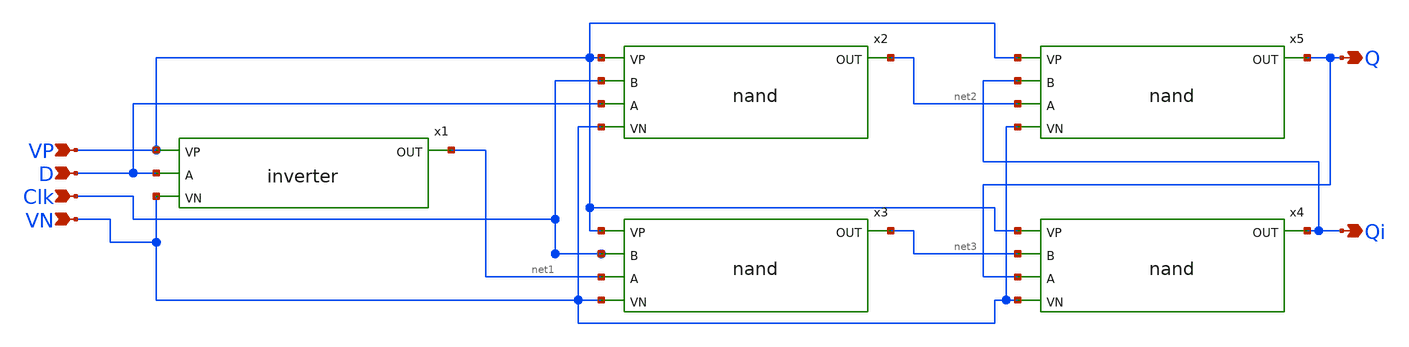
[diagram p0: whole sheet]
** sch_path: dff/xschem/dff.sch
**.subckt dff D Clk VP VN Q Qi
*.ipin D
*.ipin Clk
*.ipin VP
*.ipin VN
*.opin Q
*.opin Qi
x1 VP D net1 VN inverter
x2 VP net2 Clk D VN nand
x3 VP net3 Clk net1 VN nand
x4 VP Qi net3 Q VN nand
x5 VP Q Qi net2 VN nand
**.ends

* expanding   symbol:  /foss/designs/APIC_Mux_DFF/basic_cell/single_cell/inverter/inverter.sym # of
*+ pins=4
** sym_path: basic_cell/single_cell/inverter/inverter.sym
** sch_path: basic_cell/single_cell/inverter/inverter.sch
.subckt inverter VP A OUT VN
*.ipin A
*.ipin VP
*.ipin VN
*.opin OUT
XM1 OUT A VP VP sky130_fd_pr__pfet_01v8 L=0.15 W=3 nf=1 ad='int((nf+1)/2) * W/nf * 0.29' as='int((nf+2)/2) * W/nf * 0.29'
+ pd='2*int((nf+1)/2) * (W/nf + 0.29)' ps='2*int((nf+2)/2) * (W/nf + 0.29)' nrd='0.29 / W' nrs='0.29 / W'
+ sa=0 sb=0 sd=0 mult=1 m=1
XM2 OUT A VN VN sky130_fd_pr__nfet_01v8 L=0.15 W=1 nf=1 ad='int((nf+1)/2) * W/nf * 0.29' as='int((nf+2)/2) * W/nf * 0.29'
+ pd='2*int((nf+1)/2) * (W/nf + 0.29)' ps='2*int((nf+2)/2) * (W/nf + 0.29)' nrd='0.29 / W' nrs='0.29 / W'
+ sa=0 sb=0 sd=0 mult=1 m=1
.ends


* expanding   symbol:  /foss/designs/APIC_Mux_DFF/basic_cell/single_cell/nand/nand.sym # of pins=5
** sym_path: basic_cell/single_cell/nand/nand.sym
** sch_path: basic_cell/single_cell/nand/nand.sch
.subckt nand VP OUT B A VN
*.opin OUT
*.ipin A
*.ipin B
*.ipin VN
*.ipin VP
XM4 OUT A net1 VN sky130_fd_pr__nfet_01v8 L=0.15 W=1 nf=1 ad='int((nf+1)/2) * W/nf * 0.29' as='int((nf+2)/2) * W/nf * 0.29'
+ pd='2*int((nf+1)/2) * (W/nf + 0.29)' ps='2*int((nf+2)/2) * (W/nf + 0.29)' nrd='0.29 / W' nrs='0.29 / W'
+ sa=0 sb=0 sd=0 mult=1 m=1
XM3 net1 B VN VN sky130_fd_pr__nfet_01v8 L=0.15 W=1 nf=1 ad='int((nf+1)/2) * W/nf * 0.29' as='int((nf+2)/2) * W/nf * 0.29'
+ pd='2*int((nf+1)/2) * (W/nf + 0.29)' ps='2*int((nf+2)/2) * (W/nf + 0.29)' nrd='0.29 / W' nrs='0.29 / W'
+ sa=0 sb=0 sd=0 mult=1 m=1
XM1 OUT A VP VP sky130_fd_pr__pfet_01v8 L=0.15 W=3 nf=1 ad='int((nf+1)/2) * W/nf * 0.29' as='int((nf+2)/2) * W/nf * 0.29'
+ pd='2*int((nf+1)/2) * (W/nf + 0.29)' ps='2*int((nf+2)/2) * (W/nf + 0.29)' nrd='0.29 / W' nrs='0.29 / W'
+ sa=0 sb=0 sd=0 mult=1 m=1
XM2 OUT B VP VP sky130_fd_pr__pfet_01v8 L=0.15 W=3 nf=1 ad='int((nf+1)/2) * W/nf * 0.29' as='int((nf+2)/2) * W/nf * 0.29'
+ pd='2*int((nf+1)/2) * (W/nf + 0.29)' ps='2*int((nf+2)/2) * (W/nf + 0.29)' nrd='0.29 / W' nrs='0.29 / W'
+ sa=0 sb=0 sd=0 mult=1 m=1
.ends

.end
